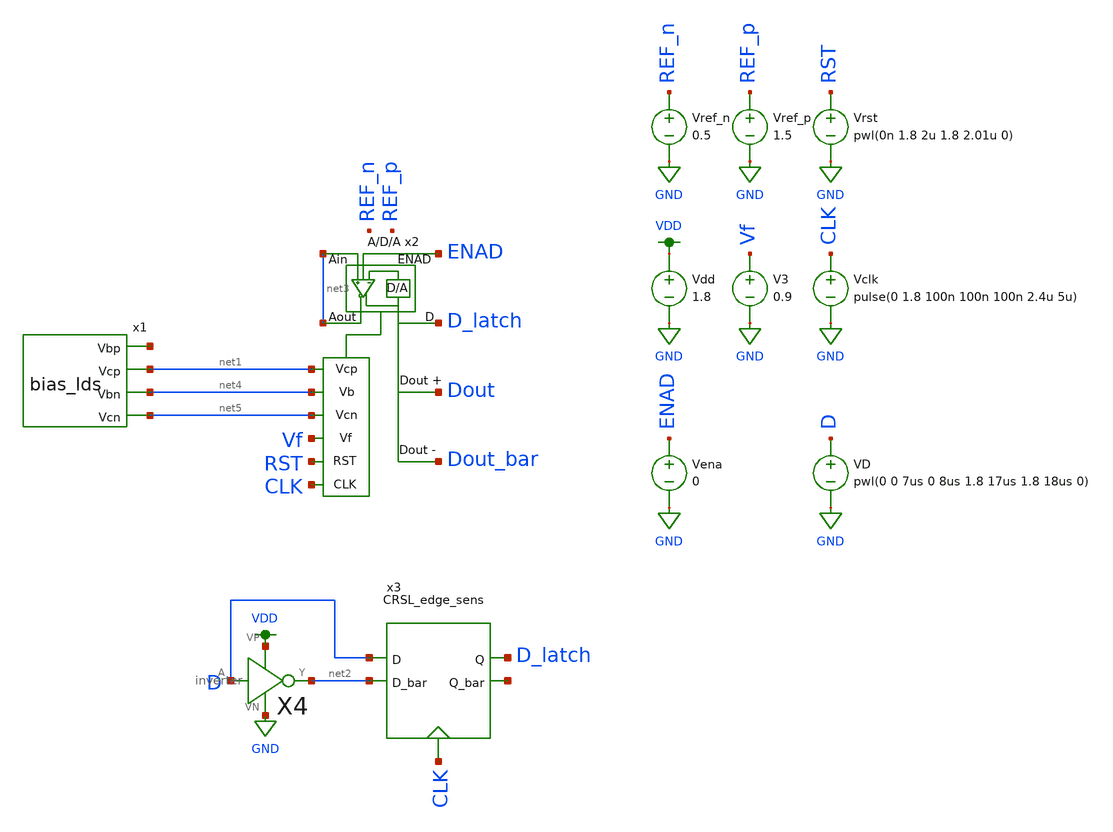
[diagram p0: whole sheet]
** sch_path: simulations/test_harness.sch
**.subckt test_harness
VD D GND pwl(0 0 7us 0 8us 1.8 17us 1.8 18us 0)
V3 Vf GND 0.9
Vena ENAD GND 0
Vrst RST GND pwl(0n 1.8 2u 1.8 2.01u 0)
Vdd VDD GND 1.8
Vclk CLK GND pulse(0 1.8 100n 100n 100n 2.4u 5u)
x2 net3 net3 D_latch ENAD net1 net4 Vf RST Dout Dout_bar net5 CLK ada_converter W_U=12 L_U0.5
x3 CLK D_latch D net7 net2 CRSL_edge_sens
X4 D net2 VDD GND inverter
Vref_n REF_n GND 0.5
Vref_p REF_p GND 1.5
**** begin user architecture code

.option wnflag=1
.param MC_SWITCH=0.0
.lib ~/skywater/skywater-pdk/libraries/sky130_fd_pr_ngspice/latest/models/sky130.lib.spice tt


.tran 1n 20u
.save all

**** end user architecture code
**.ends
.GLOBAL GND
.GLOBAL VDD
.end
